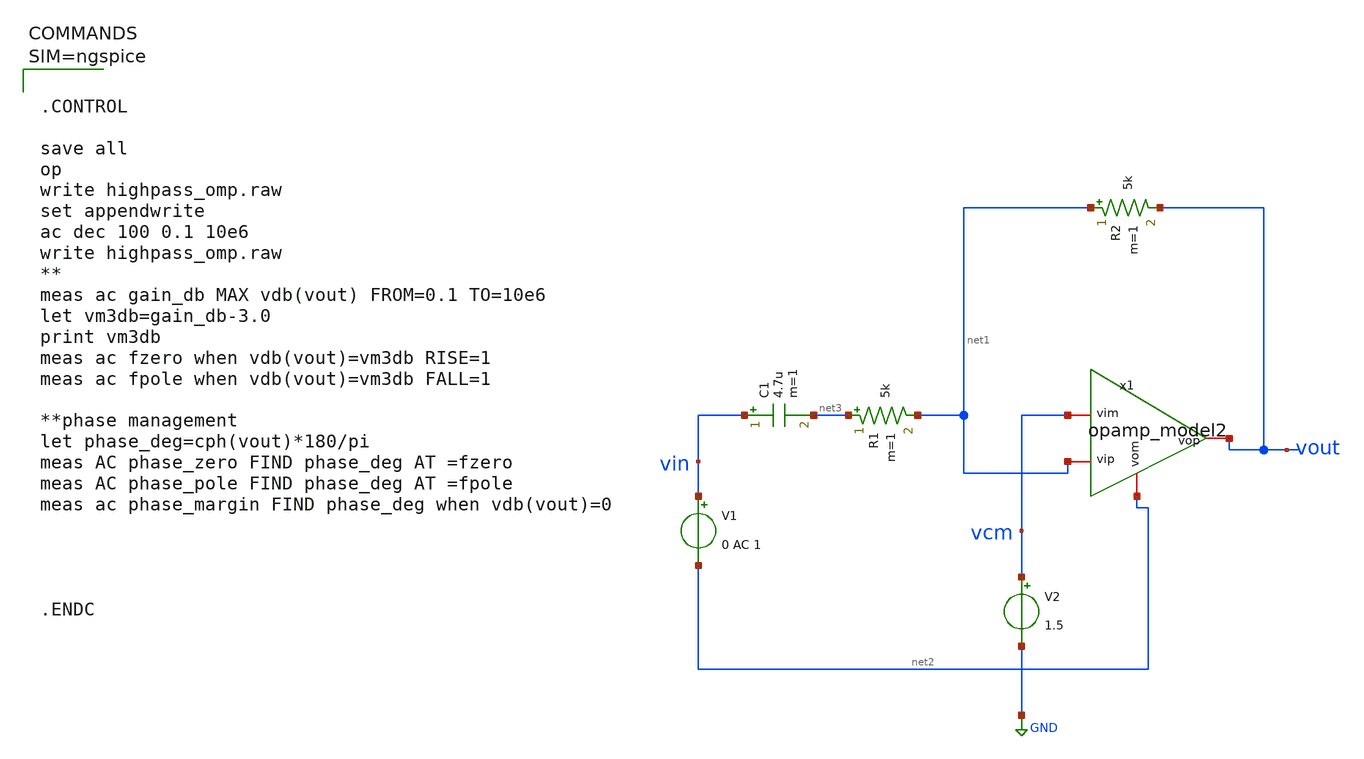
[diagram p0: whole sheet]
** sch_path: work/xschem/highpass_omp.sch
**.subckt highpass_omp
V1 vin net2 0 AC 1
R1 net3 net1 5k m=1
C1 vin net3 4.7u m=1
V2 vcm GND 1.5
R2 net1 vout 5k m=1
x1 vout net1 vcm net2 opamp_model2
**** begin user architecture code



.CONTROL

save all
op
write highpass_omp.raw
set appendwrite
ac dec 100 0.1 10e6
write highpass_omp.raw
**
meas ac gain_db MAX vdb(vout) FROM=0.1 TO=10e6
let vm3db=gain_db-3.0
print vm3db
meas ac fzero when vdb(vout)=vm3db RISE=1
meas ac fpole when vdb(vout)=vm3db FALL=1

**phase management
let phase_deg=cph(vout)*180/pi
meas AC phase_zero FIND phase_deg AT =fzero
meas AC phase_pole FIND phase_deg AT =fpole
meas ac phase_margin FIND phase_deg when vdb(vout)=0




.ENDC



**** end user architecture code
**.ends

* expanding   symbol:  opamp_model2.sym # of pins=4
** sym_path: work/xschem/opamp_model2.sym
** sch_path: work/xschem/opamp_model2.sch
.subckt opamp_model2 vop vip vim vom
*.iopin vip
*.iopin vim
*.iopin vop
*.iopin vom
E1 vop vom vip vim 1000
.ends

.GLOBAL GND
.end
